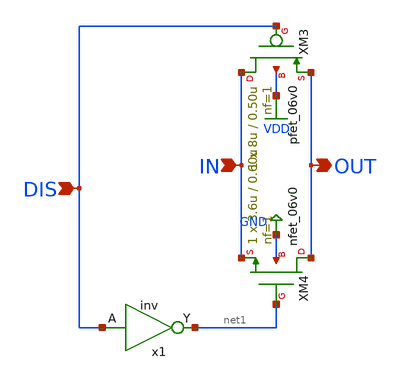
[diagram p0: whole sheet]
** sch_path: sw.sch
**.subckt sw OUT IN DIS
*.opin OUT
*.ipin IN
*.ipin DIS
XM3 IN DIS OUT VDD pfet_06v0 L=0.50u W=8u nf=1 ad='int((nf+1)/2) * W/nf * 0.18u' as='int((nf+2)/2) * W/nf * 0.18u'
+ pd='2*int((nf+1)/2) * (W/nf + 0.18u)' ps='2*int((nf+2)/2) * (W/nf + 0.18u)' nrd='0.18u / W' nrs='0.18u / W'
+ sa=0 sb=0 sd=0 m=1
XM4 OUT net1 IN GND nfet_06v0 L=0.60u W=3.6u nf=1 ad='int((nf+1)/2) * W/nf * 0.18u' as='int((nf+2)/2) * W/nf * 0.18u'
+ pd='2*int((nf+1)/2) * (W/nf + 0.18u)' ps='2*int((nf+2)/2) * (W/nf + 0.18u)' nrd='0.18u / W' nrs='0.18u / W'
+ sa=0 sb=0 sd=0 m=1
x1 DIS net1 inv
**.ends

* expanding   symbol:  inv.sym # of pins=2
** sym_path: inv.sym
** sch_path: inv.sch
.subckt inv A Y
*.opin Y
*.ipin A
XM1 Y A VDD VDD pfet_06v0 L=0.50u W=2u nf=1 ad='int((nf+1)/2) * W/nf * 0.18u' as='int((nf+2)/2) * W/nf * 0.18u'
+ pd='2*int((nf+1)/2) * (W/nf + 0.18u)' ps='2*int((nf+2)/2) * (W/nf + 0.18u)' nrd='0.18u / W' nrs='0.18u / W'
+ sa=0 sb=0 sd=0 m=1
XM2 Y A GND GND nfet_06v0 L=0.60u W=0.9u nf=1 ad='int((nf+1)/2) * W/nf * 0.18u' as='int((nf+2)/2) * W/nf * 0.18u'
+ pd='2*int((nf+1)/2) * (W/nf + 0.18u)' ps='2*int((nf+2)/2) * (W/nf + 0.18u)' nrd='0.18u / W' nrs='0.18u / W'
+ sa=0 sb=0 sd=0 m=1
.ends

.GLOBAL GND
.GLOBAL VDD
.end
